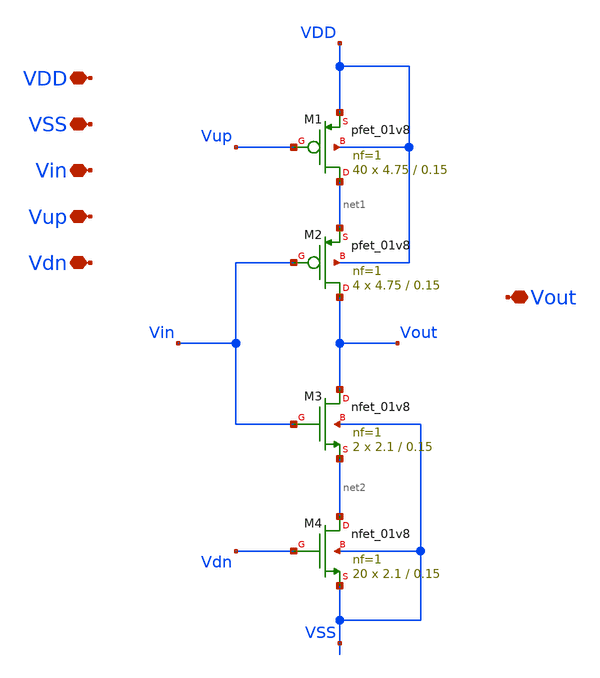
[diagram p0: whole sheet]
** sch_path: TT/tristate_inv.sch
**.subckt tristate_inv VDD VSS Vin Vout Vup Vdn
*.iopin VDD
*.iopin VSS
*.iopin Vin
*.iopin Vout
*.iopin Vup
*.iopin Vdn
XM1 net1 Vup VDD VDD sky130_fd_pr__pfet_01v8 L=0.15 W=4.75 nf=1 ad='int((nf+1)/2) * W/nf * 0.29' as='int((nf+2)/2) * W/nf * 0.29'
+ pd='2*int((nf+1)/2) * (W/nf + 0.29)' ps='2*int((nf+2)/2) * (W/nf + 0.29)' nrd='0.29 / W' nrs='0.29 / W'
+ sa=0 sb=0 sd=0 mult=40 m=40
XM2 Vout Vin net1 VDD sky130_fd_pr__pfet_01v8 L=0.15 W=4.75 nf=1 ad='int((nf+1)/2) * W/nf * 0.29' as='int((nf+2)/2) * W/nf * 0.29'
+ pd='2*int((nf+1)/2) * (W/nf + 0.29)' ps='2*int((nf+2)/2) * (W/nf + 0.29)' nrd='0.29 / W' nrs='0.29 / W'
+ sa=0 sb=0 sd=0 mult=4 m=4
XM3 Vout Vin net2 VSS sky130_fd_pr__nfet_01v8 L=0.15 W=2.1 nf=1 ad='int((nf+1)/2) * W/nf * 0.29' as='int((nf+2)/2) * W/nf * 0.29'
+ pd='2*int((nf+1)/2) * (W/nf + 0.29)' ps='2*int((nf+2)/2) * (W/nf + 0.29)' nrd='0.29 / W' nrs='0.29 / W'
+ sa=0 sb=0 sd=0 mult=2 m=2
XM4 net2 Vdn VSS VSS sky130_fd_pr__nfet_01v8 L=0.15 W=2.1 nf=1 ad='int((nf+1)/2) * W/nf * 0.29' as='int((nf+2)/2) * W/nf * 0.29'
+ pd='2*int((nf+1)/2) * (W/nf + 0.29)' ps='2*int((nf+2)/2) * (W/nf + 0.29)' nrd='0.29 / W' nrs='0.29 / W'
+ sa=0 sb=0 sd=0 mult=20 m=20
**.ends
.end
